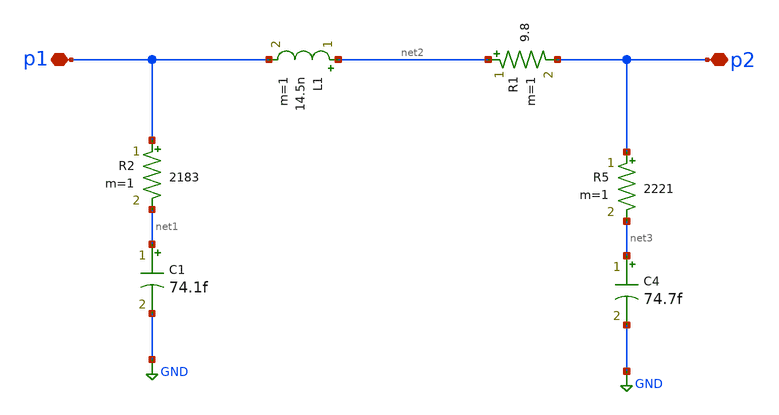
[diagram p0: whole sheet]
** sch_path: LNA7096-main/schematic/xschem/01_lna/lg.sch
**.subckt lg p1 p2
*.iopin p1
*.iopin p2
L1 net2 p1 14.5n m=1
R1 net2 p2 9.8 m=1
R2 p1 net1 2183 m=1
C1 net1 GND 74.1f m=1
R5 p2 net3 2221 m=1
C4 net3 GND 74.7f m=1
**.ends
.GLOBAL GND
.end
